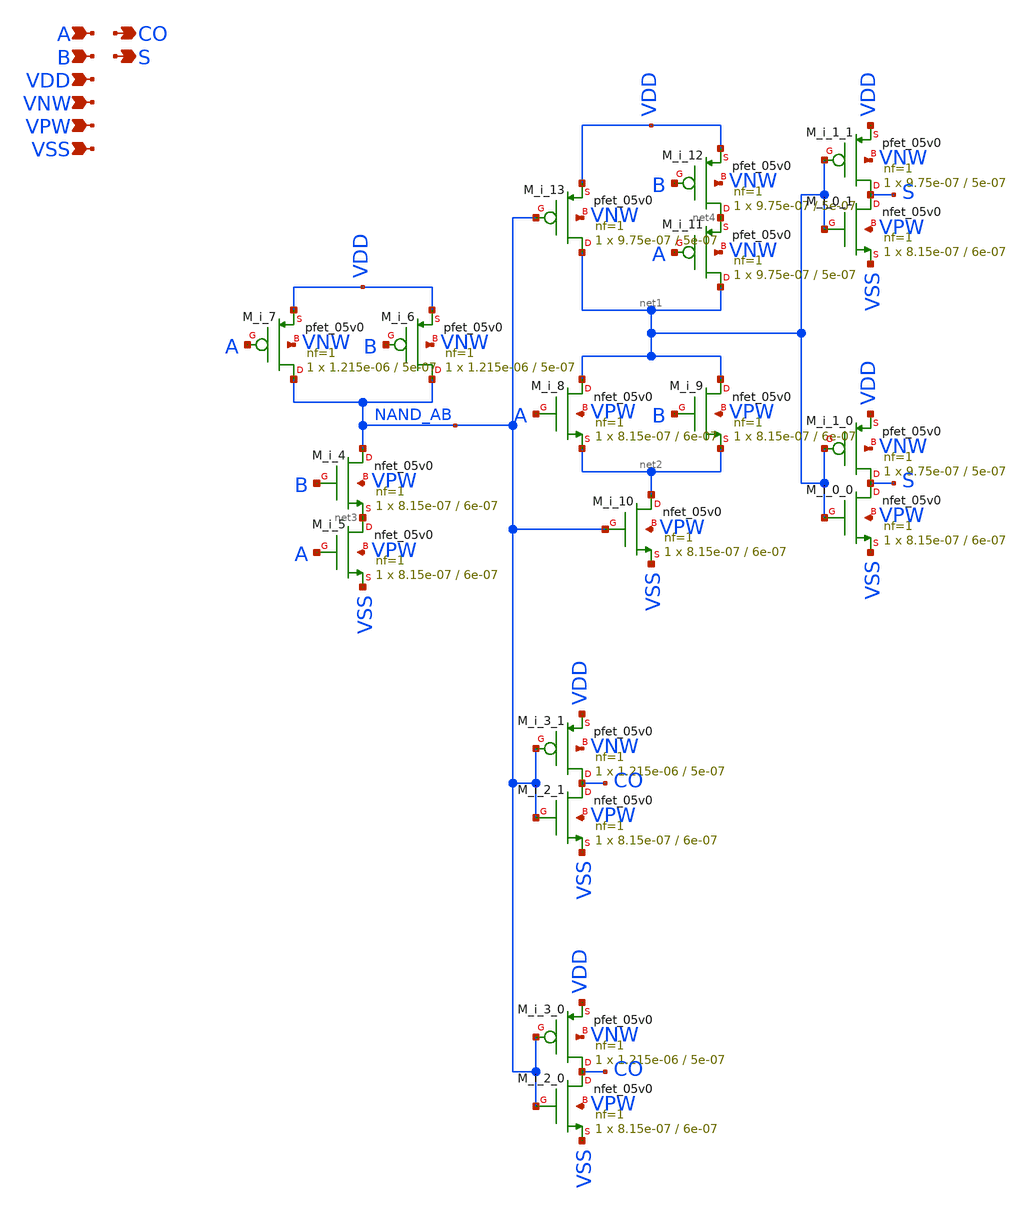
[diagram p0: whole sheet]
** sch_path: schematics/addh/gf180mcu_fd_sc_mcu7t5v0__addh_2.sch
**.subckt gf180mcu_fd_sc_mcu7t5v0__addh_2 A B CO S VDD VNW VPW VSS
*.ipin A
*.ipin B
*.opin CO
*.opin S
*.ipin VDD
*.ipin VNW
*.ipin VPW
*.ipin VSS
M_i_3_1 CO NAND_AB VDD VNW pfet_05v0 L=5e-07 W=1.215e-06 nf=1 ad='int((nf+1)/2) * W/nf * 0.18u' as='int((nf+2)/2) * W/nf * 0.18u'
+ pd='2*int((nf+1)/2) * (W/nf + 0.18u)' ps='2*int((nf+2)/2) * (W/nf + 0.18u)' nrd='0.18u / W' nrs='0.18u / W'
+ sa=0 sb=0 sd=0 m=1
M_i_2_1 CO NAND_AB VSS VPW nfet_05v0 L=6e-07 W=8.15e-07 nf=1 ad='int((nf+1)/2) * W/nf * 0.18u' as='int((nf+2)/2) * W/nf * 0.18u'
+ pd='2*int((nf+1)/2) * (W/nf + 0.18u)' ps='2*int((nf+2)/2) * (W/nf + 0.18u)' nrd='0.18u / W' nrs='0.18u / W'
+ sa=0 sb=0 sd=0 m=1
M_i_3_0 CO NAND_AB VDD VNW pfet_05v0 L=5e-07 W=1.215e-06 nf=1 ad='int((nf+1)/2) * W/nf * 0.18u' as='int((nf+2)/2) * W/nf * 0.18u'
+ pd='2*int((nf+1)/2) * (W/nf + 0.18u)' ps='2*int((nf+2)/2) * (W/nf + 0.18u)' nrd='0.18u / W' nrs='0.18u / W'
+ sa=0 sb=0 sd=0 m=1
M_i_2_0 CO NAND_AB VSS VPW nfet_05v0 L=6e-07 W=8.15e-07 nf=1 ad='int((nf+1)/2) * W/nf * 0.18u' as='int((nf+2)/2) * W/nf * 0.18u'
+ pd='2*int((nf+1)/2) * (W/nf + 0.18u)' ps='2*int((nf+2)/2) * (W/nf + 0.18u)' nrd='0.18u / W' nrs='0.18u / W'
+ sa=0 sb=0 sd=0 m=1
M_i_7 NAND_AB A VDD VNW pfet_05v0 L=5e-07 W=1.215e-06 nf=1 ad='int((nf+1)/2) * W/nf * 0.18u' as='int((nf+2)/2) * W/nf * 0.18u'
+ pd='2*int((nf+1)/2) * (W/nf + 0.18u)' ps='2*int((nf+2)/2) * (W/nf + 0.18u)' nrd='0.18u / W' nrs='0.18u / W'
+ sa=0 sb=0 sd=0 m=1
M_i_6 NAND_AB B VDD VNW pfet_05v0 L=5e-07 W=1.215e-06 nf=1 ad='int((nf+1)/2) * W/nf * 0.18u' as='int((nf+2)/2) * W/nf * 0.18u'
+ pd='2*int((nf+1)/2) * (W/nf + 0.18u)' ps='2*int((nf+2)/2) * (W/nf + 0.18u)' nrd='0.18u / W' nrs='0.18u / W'
+ sa=0 sb=0 sd=0 m=1
M_i_4 NAND_AB B net3 VPW nfet_05v0 L=6e-07 W=8.15e-07 nf=1 ad='int((nf+1)/2) * W/nf * 0.18u' as='int((nf+2)/2) * W/nf * 0.18u'
+ pd='2*int((nf+1)/2) * (W/nf + 0.18u)' ps='2*int((nf+2)/2) * (W/nf + 0.18u)' nrd='0.18u / W' nrs='0.18u / W'
+ sa=0 sb=0 sd=0 m=1
M_i_5 net3 A VSS VPW nfet_05v0 L=6e-07 W=8.15e-07 nf=1 ad='int((nf+1)/2) * W/nf * 0.18u' as='int((nf+2)/2) * W/nf * 0.18u'
+ pd='2*int((nf+1)/2) * (W/nf + 0.18u)' ps='2*int((nf+2)/2) * (W/nf + 0.18u)' nrd='0.18u / W' nrs='0.18u / W'
+ sa=0 sb=0 sd=0 m=1
M_i_13 net1 NAND_AB VDD VNW pfet_05v0 L=5e-07 W=9.75e-07 nf=1 ad='int((nf+1)/2) * W/nf * 0.18u' as='int((nf+2)/2) * W/nf * 0.18u'
+ pd='2*int((nf+1)/2) * (W/nf + 0.18u)' ps='2*int((nf+2)/2) * (W/nf + 0.18u)' nrd='0.18u / W' nrs='0.18u / W'
+ sa=0 sb=0 sd=0 m=1
M_i_12 net4 B VDD VNW pfet_05v0 L=5e-07 W=9.75e-07 nf=1 ad='int((nf+1)/2) * W/nf * 0.18u' as='int((nf+2)/2) * W/nf * 0.18u'
+ pd='2*int((nf+1)/2) * (W/nf + 0.18u)' ps='2*int((nf+2)/2) * (W/nf + 0.18u)' nrd='0.18u / W' nrs='0.18u / W'
+ sa=0 sb=0 sd=0 m=1
M_i_11 net1 A net4 VNW pfet_05v0 L=5e-07 W=9.75e-07 nf=1 ad='int((nf+1)/2) * W/nf * 0.18u' as='int((nf+2)/2) * W/nf * 0.18u'
+ pd='2*int((nf+1)/2) * (W/nf + 0.18u)' ps='2*int((nf+2)/2) * (W/nf + 0.18u)' nrd='0.18u / W' nrs='0.18u / W'
+ sa=0 sb=0 sd=0 m=1
M_i_8 net1 A net2 VPW nfet_05v0 L=6e-07 W=8.15e-07 nf=1 ad='int((nf+1)/2) * W/nf * 0.18u' as='int((nf+2)/2) * W/nf * 0.18u'
+ pd='2*int((nf+1)/2) * (W/nf + 0.18u)' ps='2*int((nf+2)/2) * (W/nf + 0.18u)' nrd='0.18u / W' nrs='0.18u / W'
+ sa=0 sb=0 sd=0 m=1
M_i_9 net1 B net2 VPW nfet_05v0 L=6e-07 W=8.15e-07 nf=1 ad='int((nf+1)/2) * W/nf * 0.18u' as='int((nf+2)/2) * W/nf * 0.18u'
+ pd='2*int((nf+1)/2) * (W/nf + 0.18u)' ps='2*int((nf+2)/2) * (W/nf + 0.18u)' nrd='0.18u / W' nrs='0.18u / W'
+ sa=0 sb=0 sd=0 m=1
M_i_10 net2 NAND_AB VSS VPW nfet_05v0 L=6e-07 W=8.15e-07 nf=1 ad='int((nf+1)/2) * W/nf * 0.18u' as='int((nf+2)/2) * W/nf * 0.18u'
+ pd='2*int((nf+1)/2) * (W/nf + 0.18u)' ps='2*int((nf+2)/2) * (W/nf + 0.18u)' nrd='0.18u / W' nrs='0.18u / W'
+ sa=0 sb=0 sd=0 m=1
M_i_1_1 S net1 VDD VNW pfet_05v0 L=5e-07 W=9.75e-07 nf=1 ad='int((nf+1)/2) * W/nf * 0.18u' as='int((nf+2)/2) * W/nf * 0.18u'
+ pd='2*int((nf+1)/2) * (W/nf + 0.18u)' ps='2*int((nf+2)/2) * (W/nf + 0.18u)' nrd='0.18u / W' nrs='0.18u / W'
+ sa=0 sb=0 sd=0 m=1
M_i_0_1 S net1 VSS VPW nfet_05v0 L=6e-07 W=8.15e-07 nf=1 ad='int((nf+1)/2) * W/nf * 0.18u' as='int((nf+2)/2) * W/nf * 0.18u'
+ pd='2*int((nf+1)/2) * (W/nf + 0.18u)' ps='2*int((nf+2)/2) * (W/nf + 0.18u)' nrd='0.18u / W' nrs='0.18u / W'
+ sa=0 sb=0 sd=0 m=1
M_i_1_0 S net1 VDD VNW pfet_05v0 L=5e-07 W=9.75e-07 nf=1 ad='int((nf+1)/2) * W/nf * 0.18u' as='int((nf+2)/2) * W/nf * 0.18u'
+ pd='2*int((nf+1)/2) * (W/nf + 0.18u)' ps='2*int((nf+2)/2) * (W/nf + 0.18u)' nrd='0.18u / W' nrs='0.18u / W'
+ sa=0 sb=0 sd=0 m=1
M_i_0_0 S net1 VSS VPW nfet_05v0 L=6e-07 W=8.15e-07 nf=1 ad='int((nf+1)/2) * W/nf * 0.18u' as='int((nf+2)/2) * W/nf * 0.18u'
+ pd='2*int((nf+1)/2) * (W/nf + 0.18u)' ps='2*int((nf+2)/2) * (W/nf + 0.18u)' nrd='0.18u / W' nrs='0.18u / W'
+ sa=0 sb=0 sd=0 m=1
**.ends
.end
